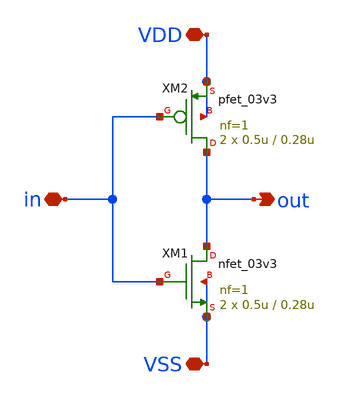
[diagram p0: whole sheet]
** sch_path: designs/sar_adc/digital/gate_inv_x2/xschem/gate_inv_x2.sch
**.subckt gate_inv_x2 out in VDD VSS
*.opin out
*.iopin in
*.iopin VDD
*.iopin VSS
XM1 out in VSS VSS nfet_03v3 L=0.28u W=0.5u nf=1 ad='int((nf+1)/2) * W/nf * 0.18u' as='int((nf+2)/2) * W/nf * 0.18u'
+ pd='2*int((nf+1)/2) * (W/nf + 0.18u)' ps='2*int((nf+2)/2) * (W/nf + 0.18u)' nrd='0.18u / W' nrs='0.18u / W'
+ sa=0 sb=0 sd=0 m=2
XM2 out in VDD VDD pfet_03v3 L=0.28u W=0.5u nf=1 ad='int((nf+1)/2) * W/nf * 0.18u' as='int((nf+2)/2) * W/nf * 0.18u'
+ pd='2*int((nf+1)/2) * (W/nf + 0.18u)' ps='2*int((nf+2)/2) * (W/nf + 0.18u)' nrd='0.18u / W' nrs='0.18u / W'
+ sa=0 sb=0 sd=0 m=2
**.ends
.end
